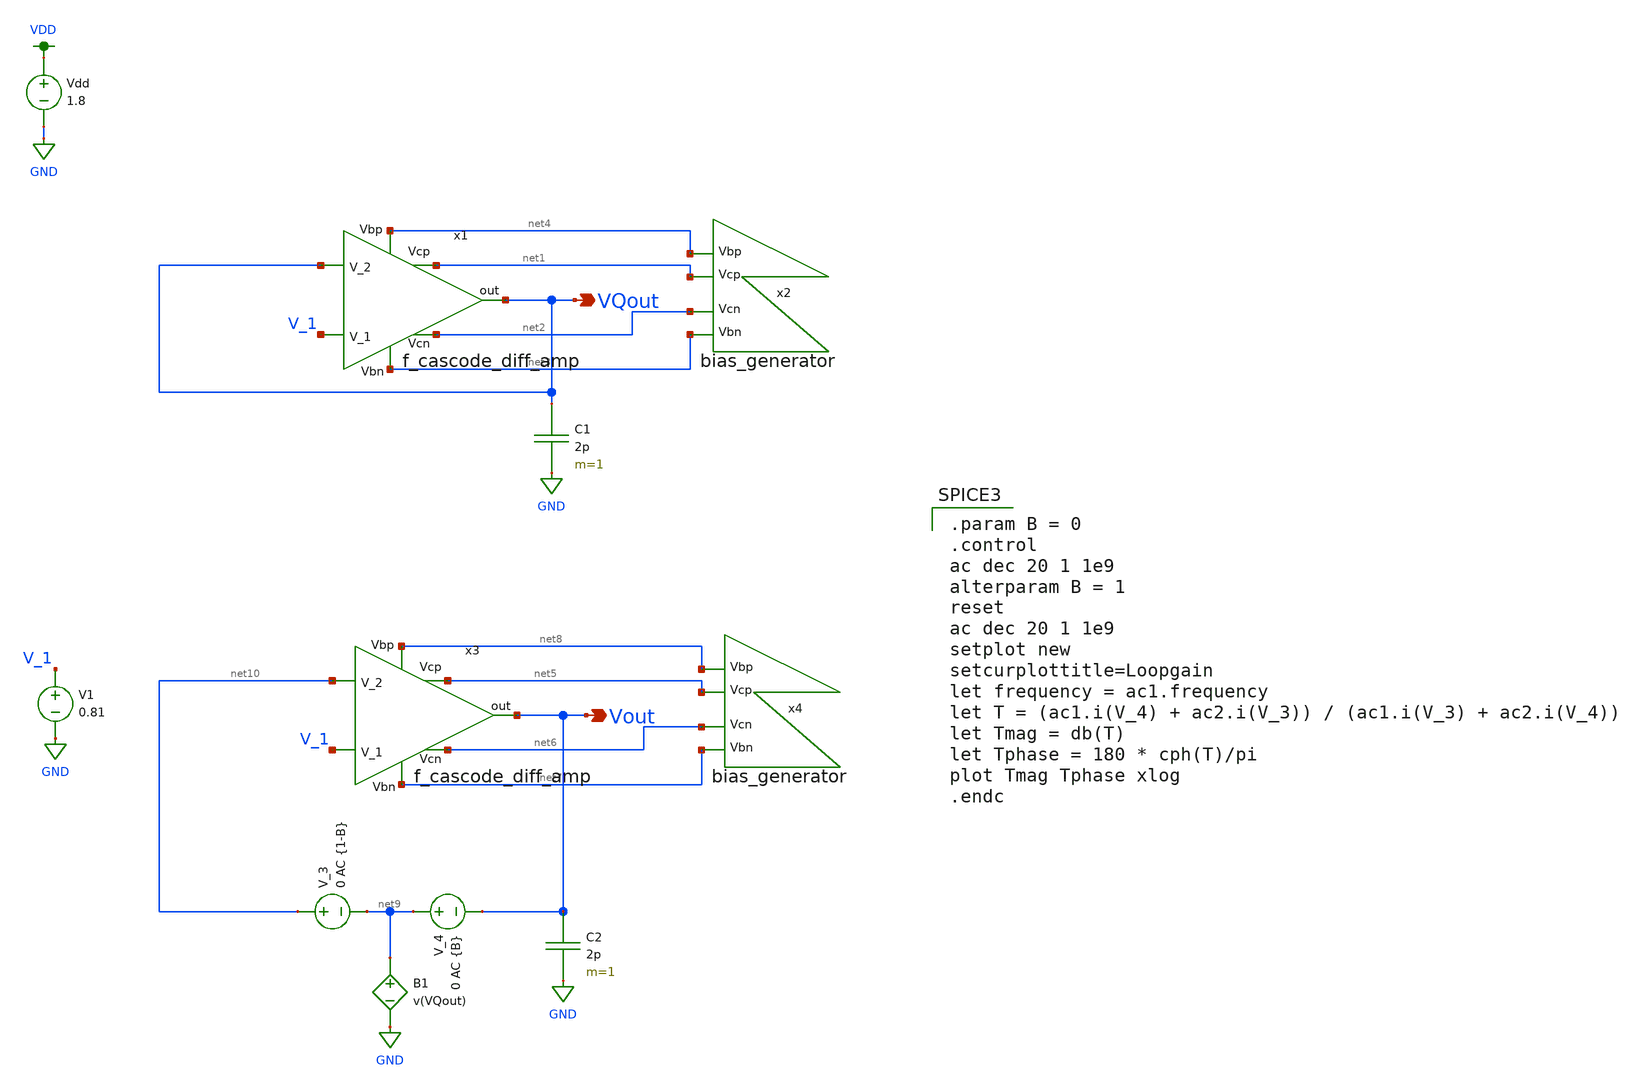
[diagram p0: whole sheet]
** sch_path: miniproject3/test_harness_q23.sch
**.subckt test_harness_q23 VQout Vout
*.opin VQout
*.opin Vout
x1 net4 net1 VQout VQout V_1 net2 net3 f_cascode_diff_amp
x2 net4 net1 net2 net3 bias_generator
Vdd VDD GND 1.8
C1 VQout GND 2p m=1
x3 net8 net5 net10 Vout V_1 net6 net7 f_cascode_diff_amp
x4 net8 net5 net6 net7 bias_generator
V_3 net10 net9 0 AC {1-B}
V_4 net9 Vout 0 AC {B}
B1 net9 GND V=v(VQout)
C2 Vout GND 2p m=1
V1 V_1 GND 0.81
**** begin user architecture code

.option wnflag=1
.lib ~/skywater/skywater-pdk/libraries/sky130_fd_pr_ngspice/latest/models/sky130.lib.spice tt


.param B = 0
.control
ac dec 20 1 1e9
alterparam B = 1
reset
ac dec 20 1 1e9
setplot new
setcurplottitle=Loopgain
let frequency = ac1.frequency
let T = (ac1.i(V_4) + ac2.i(V_3)) / (ac1.i(V_3) + ac2.i(V_4))
let Tmag = db(T)
let Tphase = 180 * cph(T)/pi
plot Tmag Tphase xlog
.endc

**** end user architecture code
**.ends

* expanding   symbol:  /home/lxbtlr/MAD/miniproject3/f_cascode_diff_amp.sym # of pins=7
** sym_path: miniproject3/f_cascode_diff_amp.sym
** sch_path: miniproject3/f_cascode_diff_amp.sch
.subckt f_cascode_diff_amp Vbp Vcp V_2 out V_1 Vcn Vbn
*.ipin V_1
*.ipin V_2
*.ipin Vcp
*.ipin Vcn
*.opin out
*.ipin Vbp
*.ipin Vbn
XM11 net4 V_2 net6 GND sky130_fd_pr__nfet_01v8 L=0.5 W=12 nf=1 ad='int((nf+1)/2) * W/nf * 0.29' as='int((nf+2)/2) * W/nf * 0.29'
+ pd='2*int((nf+1)/2) * (W/nf + 0.29)' ps='2*int((nf+2)/2) * (W/nf + 0.29)' nrd='0.29 / W' nrs='0.29 / W'
+ sa=0 sb=0 sd=0 mult=1 m=1
XM10 net5 V_1 net6 GND sky130_fd_pr__nfet_01v8 L=0.5 W=12 nf=1 ad='int((nf+1)/2) * W/nf * 0.29' as='int((nf+2)/2) * W/nf * 0.29'
+ pd='2*int((nf+1)/2) * (W/nf + 0.29)' ps='2*int((nf+2)/2) * (W/nf + 0.29)' nrd='0.29 / W' nrs='0.29 / W'
+ sa=0 sb=0 sd=0 mult=1 m=1
XM1 net6 Vbn GND GND sky130_fd_pr__nfet_01v8 L=0.5 W=12 nf=1 ad='int((nf+1)/2) * W/nf * 0.29' as='int((nf+2)/2) * W/nf * 0.29'
+ pd='2*int((nf+1)/2) * (W/nf + 0.29)' ps='2*int((nf+2)/2) * (W/nf + 0.29)' nrd='0.29 / W' nrs='0.29 / W'
+ sa=0 sb=0 sd=0 mult=1 m=1
XM8 GND net2 net1 GND sky130_fd_pr__nfet_01v8 L=0.5 W=12 nf=1 ad='int((nf+1)/2) * W/nf * 0.29' as='int((nf+2)/2) * W/nf * 0.29'
+ pd='2*int((nf+1)/2) * (W/nf + 0.29)' ps='2*int((nf+2)/2) * (W/nf + 0.29)' nrd='0.29 / W' nrs='0.29 / W'
+ sa=0 sb=0 sd=0 mult=1 m=1
XM9 net3 net2 GND GND sky130_fd_pr__nfet_01v8 L=0.5 W=12 nf=1 ad='int((nf+1)/2) * W/nf * 0.29' as='int((nf+2)/2) * W/nf * 0.29'
+ pd='2*int((nf+1)/2) * (W/nf + 0.29)' ps='2*int((nf+2)/2) * (W/nf + 0.29)' nrd='0.29 / W' nrs='0.29 / W'
+ sa=0 sb=0 sd=0 mult=1 m=1
XM7 out Vcn net3 GND sky130_fd_pr__nfet_01v8 L=0.5 W=12 nf=1 ad='int((nf+1)/2) * W/nf * 0.29' as='int((nf+2)/2) * W/nf * 0.29'
+ pd='2*int((nf+1)/2) * (W/nf + 0.29)' ps='2*int((nf+2)/2) * (W/nf + 0.29)' nrd='0.29 / W' nrs='0.29 / W'
+ sa=0 sb=0 sd=0 mult=1 m=1
XM2 net2 Vcn net1 GND sky130_fd_pr__nfet_01v8 L=0.5 W=12 nf=1 ad='int((nf+1)/2) * W/nf * 0.29' as='int((nf+2)/2) * W/nf * 0.29'
+ pd='2*int((nf+1)/2) * (W/nf + 0.29)' ps='2*int((nf+2)/2) * (W/nf + 0.29)' nrd='0.29 / W' nrs='0.29 / W'
+ sa=0 sb=0 sd=0 mult=1 m=1
XM5 net2 Vcp net5 VDD sky130_fd_pr__pfet_01v8 L=0.5 W=12 nf=1 ad='int((nf+1)/2) * W/nf * 0.29' as='int((nf+2)/2) * W/nf * 0.29'
+ pd='2*int((nf+1)/2) * (W/nf + 0.29)' ps='2*int((nf+2)/2) * (W/nf + 0.29)' nrd='0.29 / W' nrs='0.29 / W'
+ sa=0 sb=0 sd=0 mult=1 m=1
XM6 out Vcp net4 VDD sky130_fd_pr__pfet_01v8 L=0.5 W=12 nf=1 ad='int((nf+1)/2) * W/nf * 0.29' as='int((nf+2)/2) * W/nf * 0.29'
+ pd='2*int((nf+1)/2) * (W/nf + 0.29)' ps='2*int((nf+2)/2) * (W/nf + 0.29)' nrd='0.29 / W' nrs='0.29 / W'
+ sa=0 sb=0 sd=0 mult=1 m=1
XM4 net4 Vbp VDD VDD sky130_fd_pr__pfet_01v8 L=0.5 W=12 nf=1 ad='int((nf+1)/2) * W/nf * 0.29' as='int((nf+2)/2) * W/nf * 0.29'
+ pd='2*int((nf+1)/2) * (W/nf + 0.29)' ps='2*int((nf+2)/2) * (W/nf + 0.29)' nrd='0.29 / W' nrs='0.29 / W'
+ sa=0 sb=0 sd=0 mult=1 m=1
XM3 net5 Vbp VDD VDD sky130_fd_pr__pfet_01v8 L=0.5 W=12 nf=1 ad='int((nf+1)/2) * W/nf * 0.29' as='int((nf+2)/2) * W/nf * 0.29'
+ pd='2*int((nf+1)/2) * (W/nf + 0.29)' ps='2*int((nf+2)/2) * (W/nf + 0.29)' nrd='0.29 / W' nrs='0.29 / W'
+ sa=0 sb=0 sd=0 mult=1 m=1
.ends


* expanding   symbol:  /home/lxbtlr/MAD/miniproject3/bias_generator.sym # of pins=4
** sym_path: miniproject3/bias_generator.sym
** sch_path: miniproject3/bias_generator.sch
.subckt bias_generator Vbp Vcp Vcn Vbn
*.opin Vbp
*.opin Vbn
*.opin Vcp
*.opin Vcn
XM1 net2 Vbp VDD VDD sky130_fd_pr__pfet_01v8 L=2.5 W=12 nf=1 ad='int((nf+1)/2) * W/nf * 0.29' as='int((nf+2)/2) * W/nf * 0.29'
+ pd='2*int((nf+1)/2) * (W/nf + 0.29)' ps='2*int((nf+2)/2) * (W/nf + 0.29)' nrd='0.29 / W' nrs='0.29 / W'
+ sa=0 sb=0 sd=0 mult=1 m=1
XM2 Vcn Vbp VDD VDD sky130_fd_pr__pfet_01v8 L=0.5 W=12 nf=1 ad='int((nf+1)/2) * W/nf * 0.29' as='int((nf+2)/2) * W/nf * 0.29'
+ pd='2*int((nf+1)/2) * (W/nf + 0.29)' ps='2*int((nf+2)/2) * (W/nf + 0.29)' nrd='0.29 / W' nrs='0.29 / W'
+ sa=0 sb=0 sd=0 mult=1 m=1
XM3 net2 net2 net1 GND sky130_fd_pr__nfet_01v8 L=0.5 W=48 nf=1 ad='int((nf+1)/2) * W/nf * 0.29' as='int((nf+2)/2) * W/nf * 0.29'
+ pd='2*int((nf+1)/2) * (W/nf + 0.29)' ps='2*int((nf+2)/2) * (W/nf + 0.29)' nrd='0.29 / W' nrs='0.29 / W'
+ sa=0 sb=0 sd=0 mult=1 m=1
XM4 net1 Vcn Vcn GND sky130_fd_pr__nfet_01v8 L=0.5 W=12 nf=1 ad='int((nf+1)/2) * W/nf * 0.29' as='int((nf+2)/2) * W/nf * 0.29'
+ pd='2*int((nf+1)/2) * (W/nf + 0.29)' ps='2*int((nf+2)/2) * (W/nf + 0.29)' nrd='0.29 / W' nrs='0.29 / W'
+ sa=0 sb=0 sd=0 mult=1 m=1
XM5 net1 net2 GND GND sky130_fd_pr__nfet_01v8 L=0.5 W=12 nf=1 ad='int((nf+1)/2) * W/nf * 0.29' as='int((nf+2)/2) * W/nf * 0.29'
+ pd='2*int((nf+1)/2) * (W/nf + 0.29)' ps='2*int((nf+2)/2) * (W/nf + 0.29)' nrd='0.29 / W' nrs='0.29 / W'
+ sa=0 sb=0 sd=0 mult=1 m=1
XM6 net4 net3 VDD VDD sky130_fd_pr__pfet_01v8 L=0.5 W=12 nf=1 ad='int((nf+1)/2) * W/nf * 0.29' as='int((nf+2)/2) * W/nf * 0.29'
+ pd='2*int((nf+1)/2) * (W/nf + 0.29)' ps='2*int((nf+2)/2) * (W/nf + 0.29)' nrd='0.29 / W' nrs='0.29 / W'
+ sa=0 sb=0 sd=0 mult=1 m=1
XM7 net3 net3 net4 VDD sky130_fd_pr__pfet_01v8 L=0.5 W=48 nf=1 ad='int((nf+1)/2) * W/nf * 0.29' as='int((nf+2)/2) * W/nf * 0.29'
+ pd='2*int((nf+1)/2) * (W/nf + 0.29)' ps='2*int((nf+2)/2) * (W/nf + 0.29)' nrd='0.29 / W' nrs='0.29 / W'
+ sa=0 sb=0 sd=0 mult=1 m=1
XM8 net4 Vcp Vcp VDD sky130_fd_pr__pfet_01v8 L=0.5 W=12 nf=1 ad='int((nf+1)/2) * W/nf * 0.29' as='int((nf+2)/2) * W/nf * 0.29'
+ pd='2*int((nf+1)/2) * (W/nf + 0.29)' ps='2*int((nf+2)/2) * (W/nf + 0.29)' nrd='0.29 / W' nrs='0.29 / W'
+ sa=0 sb=0 sd=0 mult=1 m=1
XM9 net3 Vbn GND GND sky130_fd_pr__nfet_01v8 L=2.5 W=12 nf=1 ad='int((nf+1)/2) * W/nf * 0.29' as='int((nf+2)/2) * W/nf * 0.29'
+ pd='2*int((nf+1)/2) * (W/nf + 0.29)' ps='2*int((nf+2)/2) * (W/nf + 0.29)' nrd='0.29 / W' nrs='0.29 / W'
+ sa=0 sb=0 sd=0 mult=1 m=1
XM10 Vcp Vbn GND GND sky130_fd_pr__nfet_01v8 L=0.5 W=12 nf=1 ad='int((nf+1)/2) * W/nf * 0.29' as='int((nf+2)/2) * W/nf * 0.29'
+ pd='2*int((nf+1)/2) * (W/nf + 0.29)' ps='2*int((nf+2)/2) * (W/nf + 0.29)' nrd='0.29 / W' nrs='0.29 / W'
+ sa=0 sb=0 sd=0 mult=1 m=1
I1 GND Vbn 1u
XM11 GND Vbn Vbn GND sky130_fd_pr__nfet_01v8 L=0.5 W=12 nf=1 ad='int((nf+1)/2) * W/nf * 0.29' as='int((nf+2)/2) * W/nf * 0.29'
+ pd='2*int((nf+1)/2) * (W/nf + 0.29)' ps='2*int((nf+2)/2) * (W/nf + 0.29)' nrd='0.29 / W' nrs='0.29 / W'
+ sa=0 sb=0 sd=0 mult=1 m=1
XM12 Vbp Vbn GND GND sky130_fd_pr__nfet_01v8 L=0.5 W=12 nf=1 ad='int((nf+1)/2) * W/nf * 0.29' as='int((nf+2)/2) * W/nf * 0.29'
+ pd='2*int((nf+1)/2) * (W/nf + 0.29)' ps='2*int((nf+2)/2) * (W/nf + 0.29)' nrd='0.29 / W' nrs='0.29 / W'
+ sa=0 sb=0 sd=0 mult=1 m=1
XM13 Vbp Vbp VDD VDD sky130_fd_pr__pfet_01v8 L=0.5 W=12 nf=1 ad='int((nf+1)/2) * W/nf * 0.29' as='int((nf+2)/2) * W/nf * 0.29'
+ pd='2*int((nf+1)/2) * (W/nf + 0.29)' ps='2*int((nf+2)/2) * (W/nf + 0.29)' nrd='0.29 / W' nrs='0.29 / W'
+ sa=0 sb=0 sd=0 mult=1 m=1
.ends

.GLOBAL VDD
.GLOBAL GND
.end
